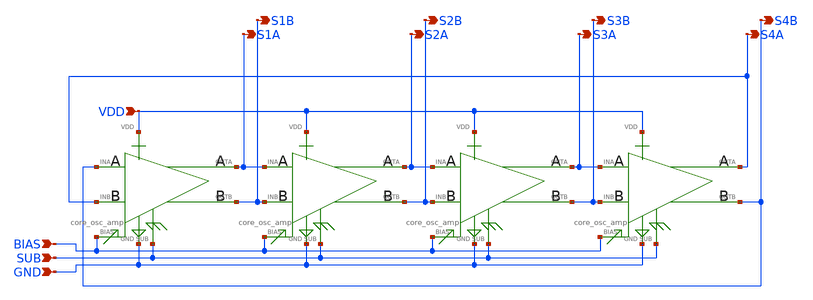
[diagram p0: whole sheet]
** sch_path: design/vco/100M~5G/core_osc.sch
**.subckt core_osc VDD BIAS SUB GND S1A S1B S2A S2B S3A S3B S4A S4B
*.ipin VDD
*.ipin BIAS
*.ipin SUB
*.ipin GND
*.opin S1A
*.opin S1B
*.opin S2A
*.opin S2B
*.opin S3A
*.opin S3B
*.opin S4A
*.opin S4B
X5 S4B S4A BIAS VDD GND SUB S1A S1B core_osc_amp
X6 S1A S1B BIAS VDD GND SUB S2A S2B core_osc_amp
X2 S2A S2B BIAS VDD GND SUB S3A S3B core_osc_amp
X7 S3A S3B BIAS VDD GND SUB S4A S4B core_osc_amp
**.ends
.end
